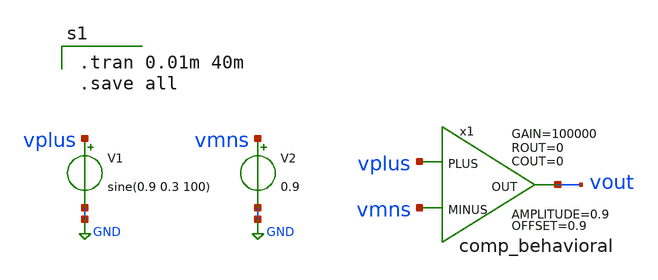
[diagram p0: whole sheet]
** sch_path: Behavioral_model/test.sch
**.subckt test
x1 vplus vmns vout comp_behavioral OFFSET=0.9 AMPLITUDE=0.9 GAIN=100000 ROUT=0 COUT=0
V1 vplus GND sine(0.9 0.3 100)
V2 vmns GND 0.9
**** begin user architecture code

.tran 0.01m 40m
.save all

**** end user architecture code
**.ends
.GLOBAL GND
.end
